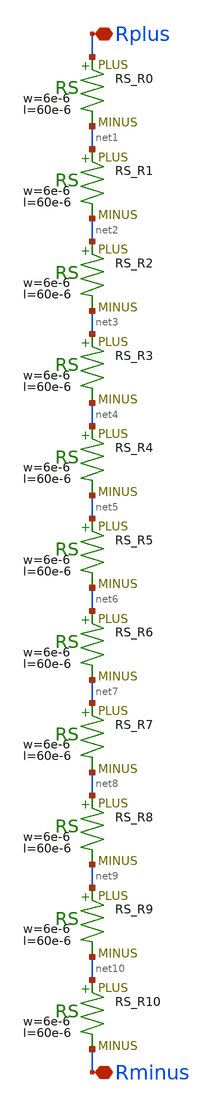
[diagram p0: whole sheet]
** sch_path: Vol.2/files/05/xschem/Vref_resistor10.sch
**.subckt Vref_resistor10 Rplus Rminus
*.iopin Rplus
*.iopin Rminus
XR0 Rplus net1 F_RS w=6e-6 R=1 l=60e-6 tc1=0 tc2=0
XR1 net1 net2 F_RS w=6e-6 R=1 l=60e-6 tc1=0 tc2=0
XR2 net2 net3 F_RS w=6e-6 R=1 l=60e-6 tc1=0 tc2=0
XR3 net3 net4 F_RS w=6e-6 R=1 l=60e-6 tc1=0 tc2=0
XR4 net4 net5 F_RS w=6e-6 R=1 l=60e-6 tc1=0 tc2=0
XR5 net5 net6 F_RS w=6e-6 R=1 l=60e-6 tc1=0 tc2=0
XR6 net6 net7 F_RS w=6e-6 R=1 l=60e-6 tc1=0 tc2=0
XR7 net7 net8 F_RS w=6e-6 R=1 l=60e-6 tc1=0 tc2=0
XR8 net8 net9 F_RS w=6e-6 R=1 l=60e-6 tc1=0 tc2=0
XR9 net9 net10 F_RS w=6e-6 R=1 l=60e-6 tc1=0 tc2=0
XR10 net10 Rminus F_RS w=6e-6 R=1 l=60e-6 tc1=0 tc2=0
**.ends
.end
